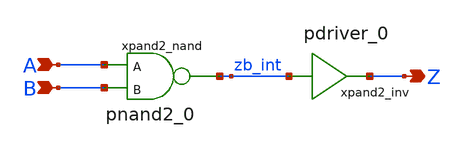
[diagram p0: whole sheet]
** sch_path: sram_2_64_scn4m_lcc/pand2_0.sch
**.subckt pand2_0 A B Z
*.ipin A
*.ipin B
*.opin Z
xpand2_nand A B zb_int vdd gnd pnand2_0
xpand2_inv zb_int Z vdd gnd pdriver_0
**** begin user architecture code


**** end user architecture code
**.ends
.end
